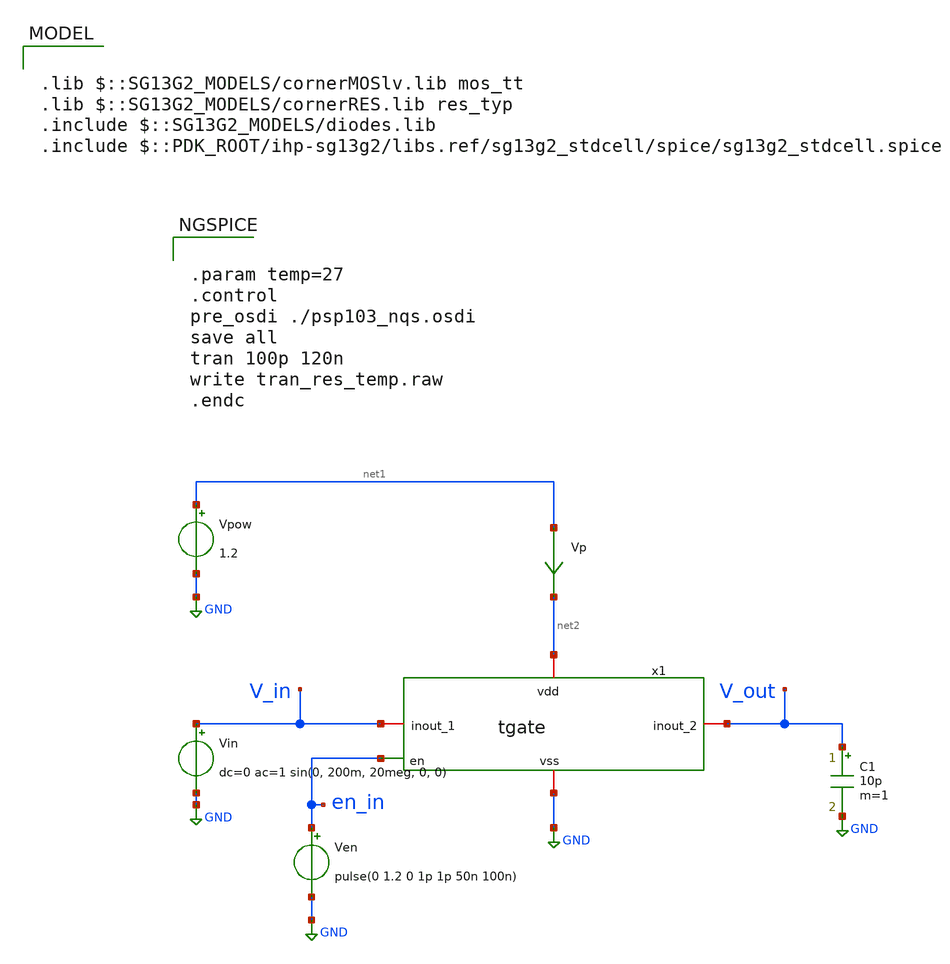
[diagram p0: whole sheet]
** sch_path: ts_pr_May2024/design_data/xschem/transmission_gate_tb.sch
* Copyright 2023 IHP PDK Authors
**.subckt transmission_gate_tb
Vpow net1 GND 1.2
Vp net1 net2 0
.save i(vp)
Vin V_in GND dc=0 ac=1 sin(0, 200m, 20meg, 0, 0)
Ven en_in GND pulse(0 1.2 0 1p 1p 50n 100n)
C1 V_out GND 10p m=1
x1 net2 V_in V_out GND en_in tgate
**** begin user architecture code

.lib $::SG13G2_MODELS/cornerMOSlv.lib mos_tt
.lib $::SG13G2_MODELS/cornerRES.lib res_typ
.include $::SG13G2_MODELS/diodes.lib
.include $::PDK_ROOT/ihp-sg13g2/libs.ref/sg13g2_stdcell/spice/sg13g2_stdcell.spice



.param temp=27
.control
pre_osdi ./psp103_nqs.osdi
save all
tran 100p 120n
write tran_res_temp.raw
.endc


**** end user architecture code
**.ends
.GLOBAL GND
.end
